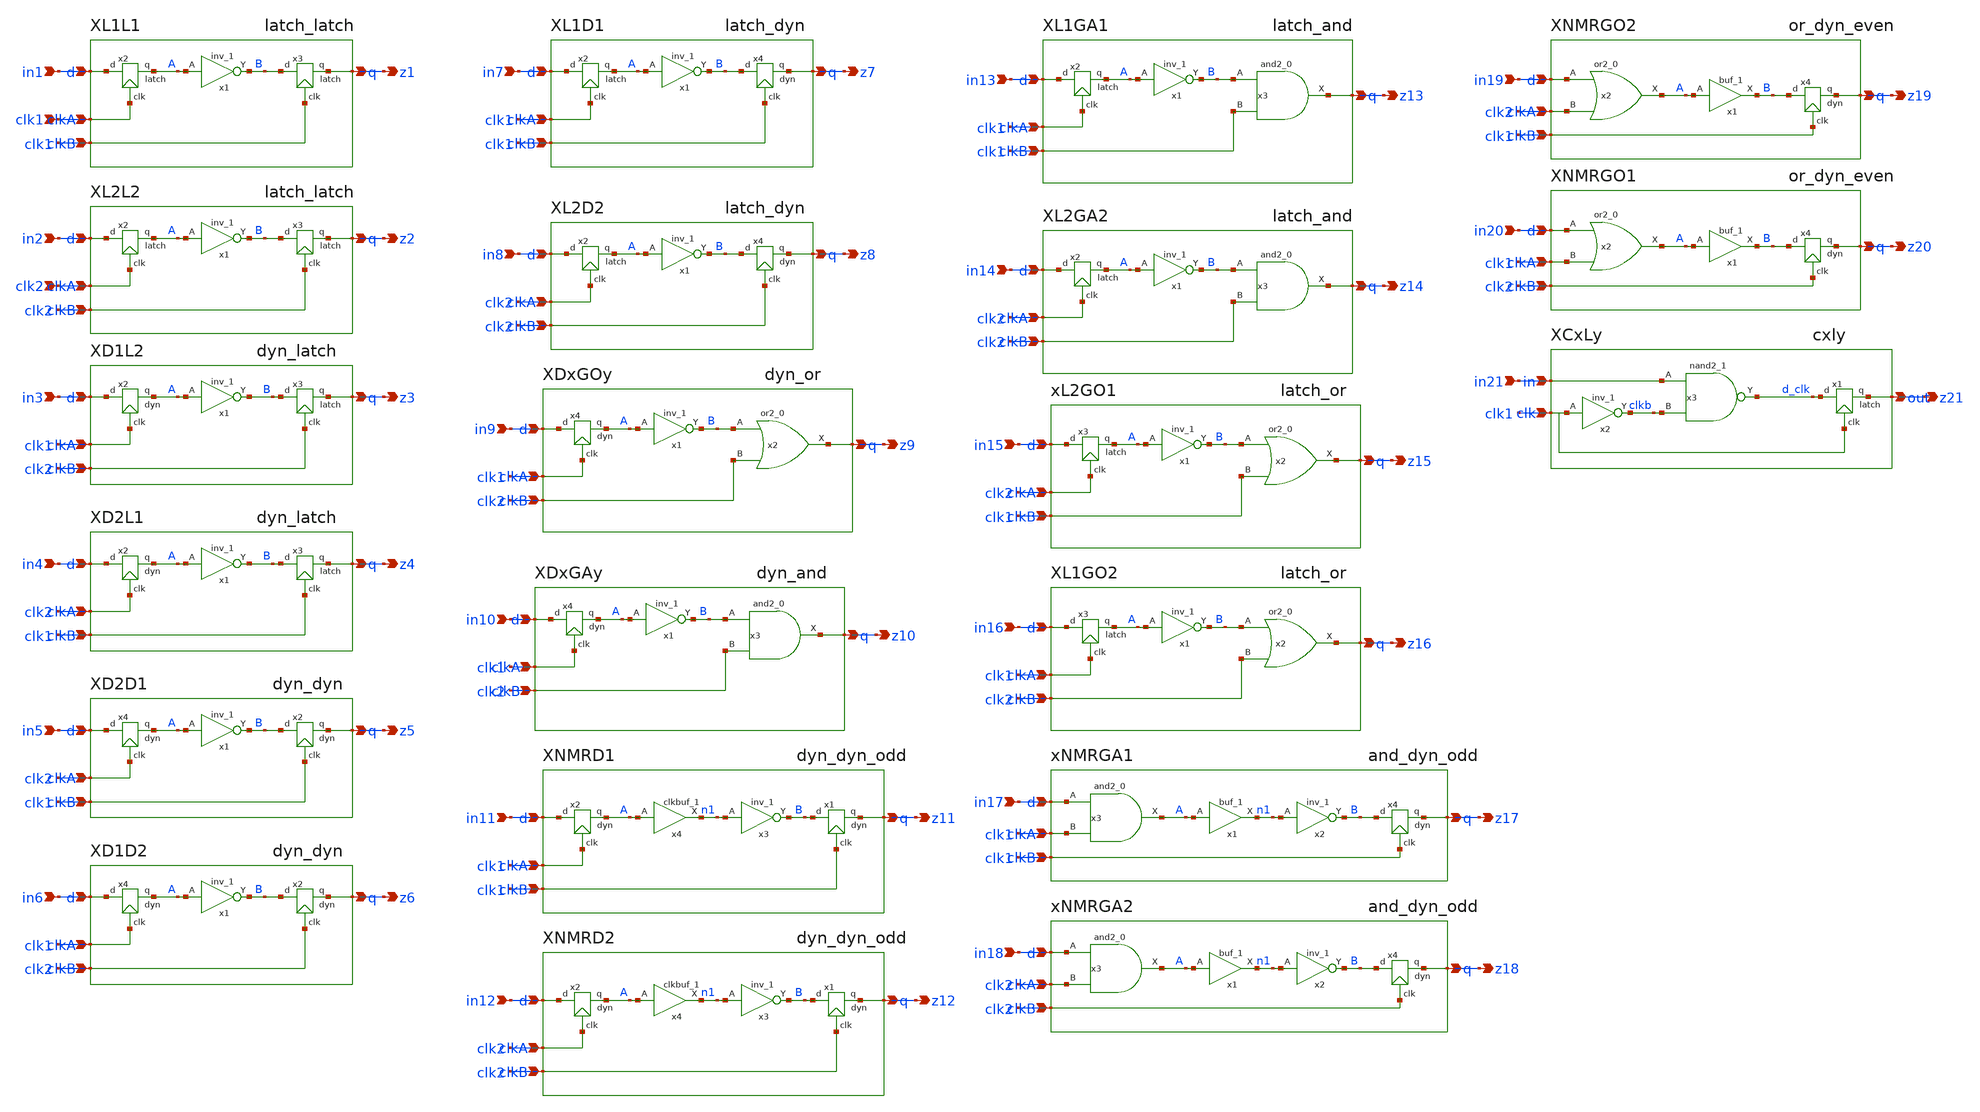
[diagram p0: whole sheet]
** sch_path: src/xe/test_cases/yxt_input_rel_test1.sch
**.subckt yxt_input_rel_test1 in1 clk1 z1 in2 z2 clk2 in3 z3 in4 z4 in5 z5 in6 z6 in7 z7 in8 z8 in9
*+ z9 in10 z10 in11 z11 in12 z12 in13 z13 in14 z14 in15 z15 in16 z16 in17 z17 in18 z18 in19 z19 in20 z20
*+ in21 z21
*.ipin in1
*.ipin clk1
*.opin z1
*.ipin in2
*.opin z2
*.ipin clk2
*.ipin in3
*.opin z3
*.ipin in4
*.opin z4
*.ipin in5
*.opin z5
*.ipin in6
*.opin z6
*.ipin in7
*.opin z7
*.ipin in8
*.opin z8
*.ipin in9
*.opin z9
*.ipin in10
*.opin z10
*.ipin in11
*.opin z11
*.ipin in12
*.opin z12
*.ipin in13
*.opin z13
*.ipin in14
*.opin z14
*.ipin in15
*.opin z15
*.ipin in16
*.opin z16
*.ipin in17
*.opin z17
*.ipin in18
*.opin z18
*.ipin in19
*.opin z19
*.ipin in20
*.opin z20
*.ipin in21
*.opin z21
XL1L1 in1 clk1 z1 clk1 latch_latch vcc=vcc vss=vss
XL2L2 in2 clk2 z2 clk2 latch_latch vcc=vcc vss=vss
XD1L2 in3 clk1 z3 clk2 dyn_latch vcc=vcc vss=vss
XD2L1 in4 clk2 z4 clk1 dyn_latch vcc=vcc vss=vss
XD2D1 in5 clk2 z5 clk1 dyn_dyn vcc=vcc vss=vss
XD1D2 in6 clk1 z6 clk2 dyn_dyn vcc=vcc vss=vss
XL1D1 in7 clk1 z7 clk1 latch_dyn vcc=vcc vss=vss
XL2D2 in8 clk2 z8 clk2 latch_dyn vcc=vcc vss=vss
XDxGOy in9 clk1 z9 clk2 dyn_or vcc=vcc vss=vss
XDxGAy in10 clk1 z10 clk2 dyn_and vcc=vcc vss=vss
XNMRD1 in11 clk1 z11 clk1 dyn_dyn_odd vcc=vcc vss=vss
XNMRD2 in12 clk2 z12 clk2 dyn_dyn_odd vcc=vcc vss=vss
XL1GA1 in13 clk1 z13 clk1 latch_and vcc=vcc vss=vss
XL2GA2 in14 clk2 z14 clk2 latch_and vcc=vcc vss=vss
xL2GO1 in15 clk2 z15 clk1 latch_or vcc=vcc vss=vss
XL1GO2 in16 clk1 z16 clk2 latch_or vcc=vcc vss=vss
xNMRGA1 in17 clk1 z17 clk1 and_dyn_odd vcc=vcc vss=vss
xNMRGA2 in18 clk2 z18 clk2 and_dyn_odd vcc=vcc vss=vss
XNMRGO2 in19 clk2 z19 clk1 or_dyn_even vcc=vcc vss=vss
XNMRGO1 in20 clk1 z20 clk2 or_dyn_even vcc=vcc vss=vss
XCxLy in21 clk1 z21 cxly vcc=vcc vss=vss
**.ends

* expanding   symbol:  yxt/latch_latch.sch # of pins=4
** sym_path: src/xe/test_cases/latch_latch.sch
** sch_path: src/xe/test_cases/latch_latch.sch
.subckt latch_latch d clkA q clkB  vcc=vcc vss=vss
*.ipin d
*.ipin clkA
*.opin q
*.ipin clkB
x1 A vcc vcc vss vss B sky130_fd_sc_hd__inv_1
x2 clkA A d latch
x3 clkB q B latch
.ends


* expanding   symbol:  yxt/dyn_latch.sch # of pins=4
** sym_path: src/xe/test_cases/dyn_latch.sch
** sch_path: src/xe/test_cases/dyn_latch.sch
.subckt dyn_latch d clkA q clkB  vcc=vcc vss=vss
*.ipin d
*.ipin clkA
*.opin q
*.ipin clkB
x1 A vcc vcc vss vss B sky130_fd_sc_hd__inv_1
x3 clkB q B latch
x2 clkA A d dyn vcc=vss vss=vss
.ends


* expanding   symbol:  yxt/dyn_dyn.sch # of pins=4
** sym_path: src/xe/test_cases/dyn_dyn.sch
** sch_path: src/xe/test_cases/dyn_dyn.sch
.subckt dyn_dyn d clkA q clkB  vcc=vcc vss=vss
*.ipin d
*.ipin clkA
*.opin q
*.ipin clkB
x1 A vcc vcc vss vss B sky130_fd_sc_hd__inv_1
x4 clkA A d dyn vcc=vss vss=vss
x2 clkB q B dyn vcc=vss vss=vss
.ends


* expanding   symbol:  yxt/latch_dyn.sch # of pins=4
** sym_path: src/xe/test_cases/latch_dyn.sch
** sch_path: src/xe/test_cases/latch_dyn.sch
.subckt latch_dyn d clkA q clkB  vcc=vcc vss=vss
*.ipin d
*.ipin clkA
*.opin q
*.ipin clkB
x1 A vcc vcc vss vss B sky130_fd_sc_hd__inv_1
x2 clkA A d latch
x4 clkB q B dyn vcc=vss vss=vss
.ends


* expanding   symbol:  yxt/dyn_or.sch # of pins=4
** sym_path: src/xe/test_cases/dyn_or.sch
** sch_path: src/xe/test_cases/dyn_or.sch
.subckt dyn_or d clkA q clkB  vcc=vcc vss=vss
*.ipin d
*.ipin clkA
*.opin q
*.ipin clkB
x1 A vcc vcc vss vss B sky130_fd_sc_hd__inv_1
x4 clkA A d dyn vcc=vss vss=vss
x2 B clkB vss vss vcc vcc q sky130_fd_sc_hd__or2_0
.ends


* expanding   symbol:  yxt/dyn_and.sch # of pins=4
** sym_path: src/xe/test_cases/dyn_and.sch
** sch_path: src/xe/test_cases/dyn_and.sch
.subckt dyn_and d clkA q clkB  vcc=vcc vss=vss
*.ipin d
*.ipin clkA
*.opin q
*.ipin clkB
x1 A vcc vcc vss vss B sky130_fd_sc_hd__inv_1
x3 B clkB vss vss vcc vcc q sky130_fd_sc_hd__and2_0
x4 clkA A d dyn vcc=vss vss=vss
.ends


* expanding   symbol:  yxt/dyn_dyn_odd.sch # of pins=4
** sym_path: src/xe/test_cases/dyn_dyn_odd.sch
** sch_path: src/xe/test_cases/dyn_dyn_odd.sch
.subckt dyn_dyn_odd d clkA q clkB  vcc=vcc vss=vss
*.ipin d
*.ipin clkA
*.opin q
*.ipin clkB
x2 clkA A d dyn vcc=vss vss=vss
x4 A vss vss vcc vcc n1 sky130_fd_sc_hd__clkbuf_1
x1 clkB q B dyn vcc=vss vss=vss
x3 n1 vss vss vcc vcc B sky130_fd_sc_hd__inv_1
.ends


* expanding   symbol:  yxt/latch_and.sch # of pins=4
** sym_path: src/xe/test_cases/latch_and.sch
** sch_path: src/xe/test_cases/latch_and.sch
.subckt latch_and d clkA q clkB  vcc=vcc vss=vss
*.ipin d
*.ipin clkA
*.opin q
*.ipin clkB
x1 A vcc vcc vss vss B sky130_fd_sc_hd__inv_1
x3 B clkB vss vss vcc vcc q sky130_fd_sc_hd__and2_0
x2 clkA A d latch
.ends


* expanding   symbol:  yxt/latch_or.sch # of pins=4
** sym_path: src/xe/test_cases/latch_or.sch
** sch_path: src/xe/test_cases/latch_or.sch
.subckt latch_or d clkA q clkB  vcc=vcc vss=vss
*.ipin d
*.ipin clkA
*.opin q
*.ipin clkB
x1 A vcc vcc vss vss B sky130_fd_sc_hd__inv_1
x2 B clkB vss vss vcc vcc q sky130_fd_sc_hd__or2_0
x3 clkA A d latch
.ends


* expanding   symbol:  yxt/and_dyn_odd.sch # of pins=4
** sym_path: src/xe/test_cases/and_dyn_odd.sch
** sch_path: src/xe/test_cases/and_dyn_odd.sch
.subckt and_dyn_odd d clkA q clkB  vcc=vcc vss=vss
*.ipin d
*.ipin clkA
*.opin q
*.ipin clkB
x4 clkB q B dyn vcc=vss vss=vss
x1 A vss vss vcc vcc n1 sky130_fd_sc_hd__buf_1
x3 d clkA VGND VNB VPB VPWR A sky130_fd_sc_hd__and2_0
x2 n1 VGND VNB VPB VPWR B sky130_fd_sc_hd__inv_1
.ends


* expanding   symbol:  yxt/or_dyn_even.sch # of pins=4
** sym_path: src/xe/test_cases/or_dyn_even.sch
** sch_path: src/xe/test_cases/or_dyn_even.sch
.subckt or_dyn_even d clkA q clkB  vcc=vcc vss=vss
*.ipin d
*.ipin clkA
*.opin q
*.ipin clkB
x2 d clkA vss vss vcc vcc A sky130_fd_sc_hd__or2_0
x4 clkB q B dyn vcc=vss vss=vss
x1 A vss vss vcc vcc B sky130_fd_sc_hd__buf_1
.ends


* expanding   symbol:  yxt/cxly.sch # of pins=3
** sym_path: src/xe/test_cases/cxly.sch
** sch_path: src/xe/test_cases/cxly.sch
.subckt cxly in clk out  vcc=vcc vss=vss
*.ipin in
*.ipin clk
*.opin out
x2 clk VGND VNB VPB VPWR clkb sky130_fd_sc_hd__inv_1
x1 clk out d_clk latch
x3 in clkb vss vss vcc vcc d_clk sky130_fd_sc_hd__nand2_1
.ends


* expanding   symbol:  yxt/latch.sym # of pins=3
** sym_path: src/xe/test_cases/latch.sym
** sch_path: src/xe/test_cases/latch.sch
.subckt latch clk q d  vcc=vcc vss=vss
*.ipin clk
*.ipin d
*.opin q
x1 d vcc vcc vss vss db sky130_fd_sc_hd__inv_1
x2 clkb db z clk tgate vcc=vcc vss=vss
x3 z vcc vcc vss vss q sky130_fd_sc_hd__inv_1
x6 clk vcc vcc vss vss clkb sky130_fd_sc_hd__inv_1
x4 z vcc vcc vss vss fb sky130_fd_sc_hd__inv_1
x5 fb vcc vcc vss vss z sky130_fd_sc_hd__inv_1
.ends


* expanding   symbol:  yxt/dyn.sym # of pins=3
** sym_path: src/xe/test_cases/dyn.sym
** sch_path: src/xe/test_cases/dyn.sch
.subckt dyn clk q d  vcc=vss vss=vss
*.ipin clk
*.opin q
*.ipin d
x1 net1 vcc vcc vss vss q sky130_fd_sc_hd__inv_1
XM1 net1 d net2 net3 sky130_fd_pr__nfet_01v8 L=0.15 W=1 nf=1 ad='int((nf+1)/2) * W/nf * 0.29' as='int((nf+2)/2) * W/nf * 0.29'
+ pd='2*int((nf+1)/2) * (W/nf + 0.29)' ps='2*int((nf+2)/2) * (W/nf + 0.29)' nrd='0.29 / W' nrs='0.29 / W'
+ sa=0 sb=0 sd=0 mult=1 m=1
XM2 net1 q vcc net4 sky130_fd_pr__pfet_01v8 L=0.15 W=1 nf=1 ad='int((nf+1)/2) * W/nf * 0.29' as='int((nf+2)/2) * W/nf * 0.29'
+ pd='2*int((nf+1)/2) * (W/nf + 0.29)' ps='2*int((nf+2)/2) * (W/nf + 0.29)' nrd='0.29 / W' nrs='0.29 / W'
+ sa=0 sb=0 sd=0 mult=1 m=1
XM3 net1 clk vcc net5 sky130_fd_pr__pfet_01v8 L=0.15 W=1 nf=1 ad='int((nf+1)/2) * W/nf * 0.29' as='int((nf+2)/2) * W/nf * 0.29'
+ pd='2*int((nf+1)/2) * (W/nf + 0.29)' ps='2*int((nf+2)/2) * (W/nf + 0.29)' nrd='0.29 / W' nrs='0.29 / W'
+ sa=0 sb=0 sd=0 mult=1 m=1
XM4 net2 clk vss net6 sky130_fd_pr__nfet_01v8 L=0.15 W=1 nf=1 ad='int((nf+1)/2) * W/nf * 0.29' as='int((nf+2)/2) * W/nf * 0.29'
+ pd='2*int((nf+1)/2) * (W/nf + 0.29)' ps='2*int((nf+2)/2) * (W/nf + 0.29)' nrd='0.29 / W' nrs='0.29 / W'
+ sa=0 sb=0 sd=0 mult=1 m=1
.ends


* expanding   symbol:  yxt/tgate.sym # of pins=4
** sym_path: src/xe/test_cases/tgate.sym
** sch_path: src/xe/test_cases/tgate.sch
.subckt tgate gp s d gn  vcc=vcc vss=vss
*.ipin s
*.ipin gp
*.ipin gn
*.opin d
XMpc d gp s vss sky130_fd_pr__pfet_01v8 L=0.15 W=1 nf=1 ad='int((nf+1)/2) * W/nf * 0.29' as='int((nf+2)/2) * W/nf * 0.29'
+ pd='2*int((nf+1)/2) * (W/nf + 0.29)' ps='2*int((nf+2)/2) * (W/nf + 0.29)' nrd='0.29 / W' nrs='0.29 / W'
+ sa=0 sb=0 sd=0 mult=7 m=7
XM15 s gn d vcc sky130_fd_pr__nfet_01v8 L=0.15 W=1 nf=1 ad='int((nf+1)/2) * W/nf * 0.29' as='int((nf+2)/2) * W/nf * 0.29'
+ pd='2*int((nf+1)/2) * (W/nf + 0.29)' ps='2*int((nf+2)/2) * (W/nf + 0.29)' nrd='0.29 / W' nrs='0.29 / W'
+ sa=0 sb=0 sd=0 mult=1 m=1
.ends

.end
